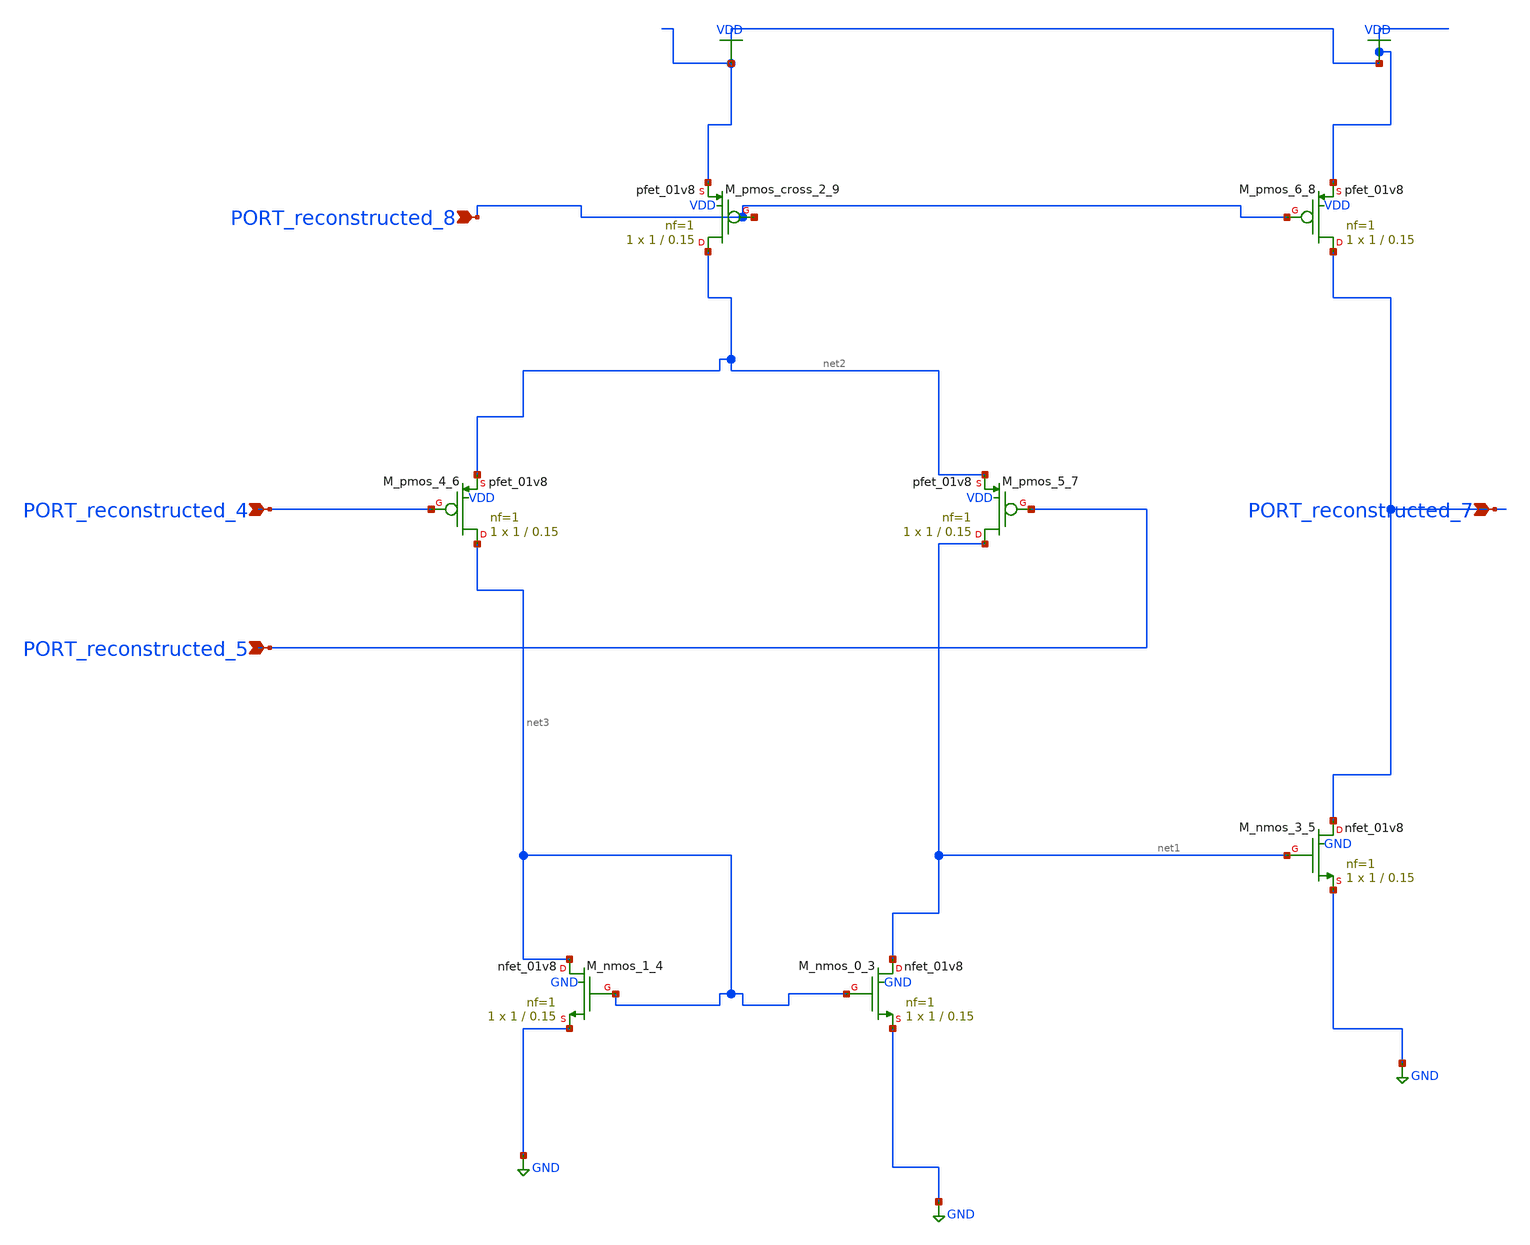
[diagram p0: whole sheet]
** sch_path: schematics/AMSNet/714.sch
**.subckt 714 PORT_reconstructed_5 PORT_reconstructed_7 PORT_reconstructed_4 PORT_reconstructed_8
*.ipin PORT_reconstructed_5
*.ipin PORT_reconstructed_7
*.ipin PORT_reconstructed_4
*.ipin PORT_reconstructed_8
XM_nmos_0_3 net1 net3 GND GND sky130_fd_pr__nfet_01v8 L=0.15 W=1 nf=1 ad='int((1 + 1)/2) * 1 / 1 * 0.29'
+ as='int((1 + 2)/2) * 1 / 1 * 0.29' pd='2*int((1 + 1)/2) * (1 / 1 + 0.29)' ps='2*int((1 + 2)/2) * (1 / 1 + 0.29)'
+ nrd='0.29 / 1 ' nrs='0.29 / 1 ' sa=0 sb=0 sd=0 mult=1 m=1
XM_nmos_1_4 net3 net3 GND GND sky130_fd_pr__nfet_01v8 L=0.15 W=1 nf=1 ad='int((1 + 1)/2) * 1 / 1 * 0.29'
+ as='int((1 + 2)/2) * 1 / 1 * 0.29' pd='2*int((1 + 1)/2) * (1 / 1 + 0.29)' ps='2*int((1 + 2)/2) * (1 / 1 + 0.29)'
+ nrd='0.29 / 1 ' nrs='0.29 / 1 ' sa=0 sb=0 sd=0 mult=1 m=1
XM_nmos_3_5 PORT_reconstructed_7 net1 GND GND sky130_fd_pr__nfet_01v8 L=0.15 W=1 nf=1 ad='int((1 + 1)/2) * 1 / 1 * 0.29'
+ as='int((1 + 2)/2) * 1 / 1 * 0.29' pd='2*int((1 + 1)/2) * (1 / 1 + 0.29)' ps='2*int((1 + 2)/2) * (1 / 1 + 0.29)'
+ nrd='0.29 / 1 ' nrs='0.29 / 1 ' sa=0 sb=0 sd=0 mult=1 m=1
XM_pmos_4_6 net3 PORT_reconstructed_4 net2 VDD sky130_fd_pr__pfet_01v8 L=0.15 W=1 nf=1 ad='int((1 + 1)/2) * 1 / 1 * 0.29'
+ as='int((1 + 2)/2) * 1 / 1 * 0.29' pd='2*int((1 + 1)/2) * (1 / 1 + 0.29)' ps='2*int((1 + 2)/2) * (1 / 1 + 0.29)'
+ nrd='0.29 / 1 ' nrs='0.29 / 1 ' sa=0 sb=0 sd=0 mult=1 m=1
XM_pmos_5_7 net1 PORT_reconstructed_5 net2 VDD sky130_fd_pr__pfet_01v8 L=0.15 W=1 nf=1 ad='int((1 + 1)/2) * 1 / 1 * 0.29'
+ as='int((1 + 2)/2) * 1 / 1 * 0.29' pd='2*int((1 + 1)/2) * (1 / 1 + 0.29)' ps='2*int((1 + 2)/2) * (1 / 1 + 0.29)'
+ nrd='0.29 / 1 ' nrs='0.29 / 1 ' sa=0 sb=0 sd=0 mult=1 m=1
XM_pmos_6_8 PORT_reconstructed_7 PORT_reconstructed_8 VDD VDD sky130_fd_pr__pfet_01v8 L=0.15 W=1 nf=1
+ ad='int((1 + 1)/2) * 1 / 1 * 0.29' as='int((1 + 2)/2) * 1 / 1 * 0.29' pd='2*int((1 + 1)/2) * (1 / 1 + 0.29)'
+ ps='2*int((1 + 2)/2) * (1 / 1 + 0.29)' nrd='0.29 / 1 ' nrs='0.29 / 1 ' sa=0 sb=0 sd=0 mult=1 m=1
XM_pmos_cross_2_9 net2 PORT_reconstructed_8 VDD VDD sky130_fd_pr__pfet_01v8 L=0.15 W=1 nf=1 ad='int((1 + 1)/2) * 1 / 1 * 0.29'
+ as='int((1 + 2)/2) * 1 / 1 * 0.29' pd='2*int((1 + 1)/2) * (1 / 1 + 0.29)' ps='2*int((1 + 2)/2) * (1 / 1 + 0.29)'
+ nrd='0.29 / 1 ' nrs='0.29 / 1 ' sa=0 sb=0 sd=0 mult=1 m=1
**.ends
.GLOBAL GND
.GLOBAL VDD
.end
